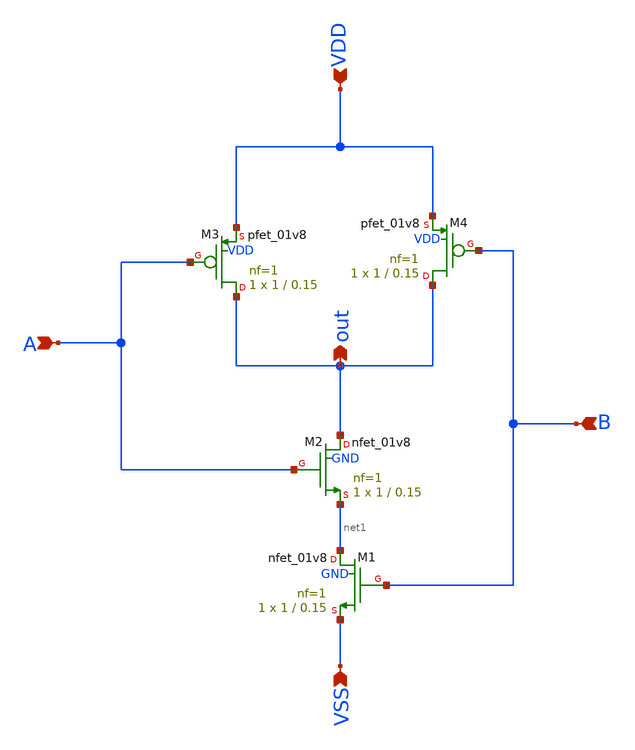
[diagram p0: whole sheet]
** sch_path: 2_bit_current_steering_DAC/nand.sch
**.subckt nand A VDD B VSS out
*.ipin A
*.ipin VDD
*.ipin B
*.ipin VSS
*.opin out
XM1 net1 B VSS GND sky130_fd_pr__nfet_01v8 L=0.15 W=1 nf=1 ad='int((1 + 1)/2) * 1 / 1 * 0.29' as='int((1 + 2)/2) * 1 / 1 * 0.29'
+ pd='2*int((1 + 1)/2) * (1 / 1 + 0.29)' ps='2*int((1 + 2)/2) * (1 / 1 + 0.29)' nrd='0.29 / 1 ' nrs='0.29 / 1 '
+ sa=0 sb=0 sd=0 mult=1 m=1
XM2 out A net1 GND sky130_fd_pr__nfet_01v8 L=0.15 W=1 nf=1 ad='int((1 + 1)/2) * 1 / 1 * 0.29' as='int((1 + 2)/2) * 1 / 1 * 0.29'
+ pd='2*int((1 + 1)/2) * (1 / 1 + 0.29)' ps='2*int((1 + 2)/2) * (1 / 1 + 0.29)' nrd='0.29 / 1 ' nrs='0.29 / 1 '
+ sa=0 sb=0 sd=0 mult=1 m=1
XM3 out A VDD VDD sky130_fd_pr__pfet_01v8 L=0.15 W=1 nf=1 ad='int((1 + 1)/2) * 1 / 1 * 0.29' as='int((1 + 2)/2) * 1 / 1 * 0.29'
+ pd='2*int((1 + 1)/2) * (1 / 1 + 0.29)' ps='2*int((1 + 2)/2) * (1 / 1 + 0.29)' nrd='0.29 / 1 ' nrs='0.29 / 1 '
+ sa=0 sb=0 sd=0 mult=1 m=1
XM4 out B VDD VDD sky130_fd_pr__pfet_01v8 L=0.15 W=1 nf=1 ad='int((1 + 1)/2) * 1 / 1 * 0.29' as='int((1 + 2)/2) * 1 / 1 * 0.29'
+ pd='2*int((1 + 1)/2) * (1 / 1 + 0.29)' ps='2*int((1 + 2)/2) * (1 / 1 + 0.29)' nrd='0.29 / 1 ' nrs='0.29 / 1 '
+ sa=0 sb=0 sd=0 mult=1 m=1
**.ends
.end
